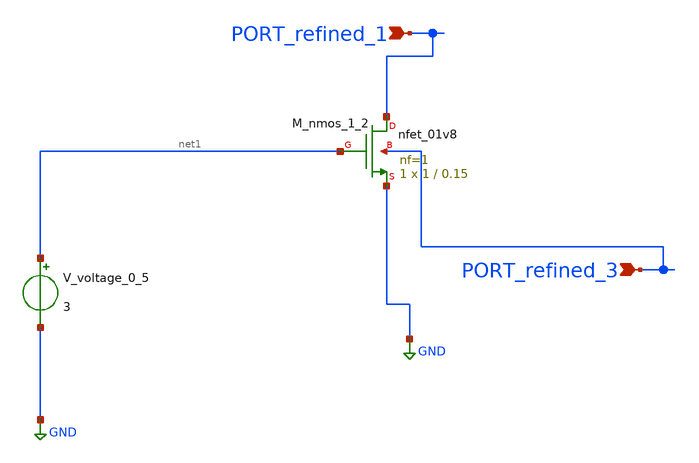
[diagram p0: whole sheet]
** sch_path: schematics/AMSNet/10.sch
**.subckt 10 PORT_refined_1 PORT_refined_3
*.ipin PORT_refined_1
*.ipin PORT_refined_3
XM_nmos_1_2 PORT_refined_1 net1 GND PORT_refined_3 sky130_fd_pr__nfet_01v8 L=0.15 W=1 nf=1 ad='int((1 + 1)/2) * 1 / 1 * 0.29'
+ as='int((1 + 2)/2) * 1 / 1 * 0.29' pd='2*int((1 + 1)/2) * (1 / 1 + 0.29)' ps='2*int((1 + 2)/2) * (1 / 1 + 0.29)'
+ nrd='0.29 / 1 ' nrs='0.29 / 1 ' sa=0 sb=0 sd=0 mult=1 m=1
V_voltage_0_5 net1 GND 3
**.ends
.GLOBAL GND
.end
